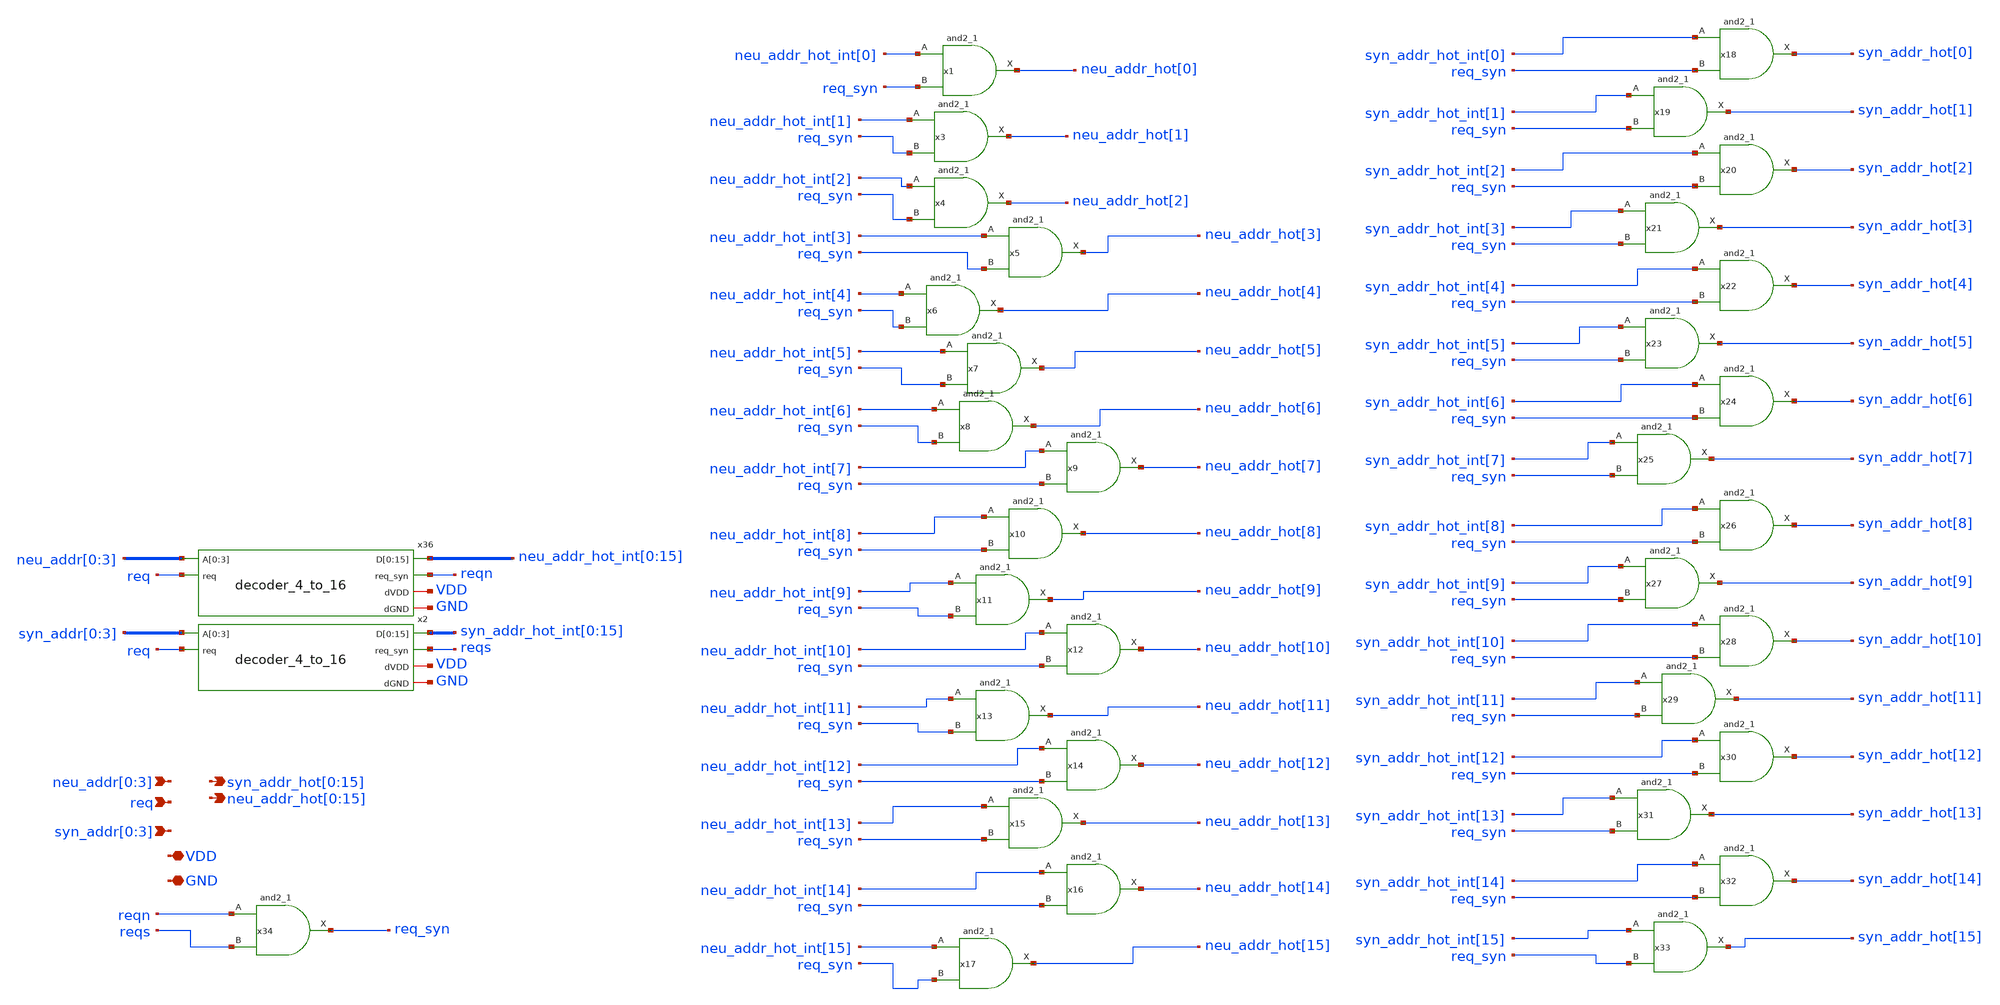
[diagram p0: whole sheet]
** sch_path: design/xschem/neu_syn_addr_decoder.sch
**.subckt neu_syn_addr_decoder neu_addr[0],neu_addr[1],neu_addr[2],neu_addr[3] req
*+ syn_addr_hot[0],syn_addr_hot[1],syn_addr_hot[2],syn_addr_hot[3],syn_addr_hot[4],syn_addr_hot[5],syn_addr_hot[6],syn_addr_hot[7],syn_addr_hot[8],syn_addr_hot[9],syn_addr_hot[10],syn_addr_hot[11],syn_addr_hot[12],syn_addr_hot[13],syn_addr_hot[14],syn_addr_hot[15] syn_addr[0],syn_addr[1],syn_addr[2],syn_addr[3]
*+ neu_addr_hot[0],neu_addr_hot[1],neu_addr_hot[2],neu_addr_hot[3],neu_addr_hot[4],neu_addr_hot[5],neu_addr_hot[6],neu_addr_hot[7],neu_addr_hot[8],neu_addr_hot[9],neu_addr_hot[10],neu_addr_hot[11],neu_addr_hot[12],neu_addr_hot[13],neu_addr_hot[14],neu_addr_hot[15] VDD GND
*.ipin neu_addr[0],neu_addr[1],neu_addr[2],neu_addr[3]
*.ipin req
*.opin
*+ syn_addr_hot[0],syn_addr_hot[1],syn_addr_hot[2],syn_addr_hot[3],syn_addr_hot[4],syn_addr_hot[5],syn_addr_hot[6],syn_addr_hot[7],syn_addr_hot[8],syn_addr_hot[9],syn_addr_hot[10],syn_addr_hot[11],syn_addr_hot[12],syn_addr_hot[13],syn_addr_hot[14],syn_addr_hot[15]
*.ipin syn_addr[0],syn_addr[1],syn_addr[2],syn_addr[3]
*.opin
*+ neu_addr_hot[0],neu_addr_hot[1],neu_addr_hot[2],neu_addr_hot[3],neu_addr_hot[4],neu_addr_hot[5],neu_addr_hot[6],neu_addr_hot[7],neu_addr_hot[8],neu_addr_hot[9],neu_addr_hot[10],neu_addr_hot[11],neu_addr_hot[12],neu_addr_hot[13],neu_addr_hot[14],neu_addr_hot[15]
*.iopin VDD
*.iopin GND
x36 neu_addr[0] neu_addr[1] neu_addr[2] neu_addr[3] neu_addr_hot_int[0] neu_addr_hot_int[1]
+ neu_addr_hot_int[2] neu_addr_hot_int[3] neu_addr_hot_int[4] neu_addr_hot_int[5] neu_addr_hot_int[6] neu_addr_hot_int[7]
+ neu_addr_hot_int[8] neu_addr_hot_int[9] neu_addr_hot_int[10] neu_addr_hot_int[11] neu_addr_hot_int[12]
+ neu_addr_hot_int[13] neu_addr_hot_int[14] neu_addr_hot_int[15] req reqn VDD GND decoder_4_to_16
x2 syn_addr[0] syn_addr[1] syn_addr[2] syn_addr[3] syn_addr_hot_int[0] syn_addr_hot_int[1]
+ syn_addr_hot_int[2] syn_addr_hot_int[3] syn_addr_hot_int[4] syn_addr_hot_int[5] syn_addr_hot_int[6] syn_addr_hot_int[7]
+ syn_addr_hot_int[8] syn_addr_hot_int[9] syn_addr_hot_int[10] syn_addr_hot_int[11] syn_addr_hot_int[12]
+ syn_addr_hot_int[13] syn_addr_hot_int[14] syn_addr_hot_int[15] req reqs VDD GND decoder_4_to_16
x1 neu_addr_hot_int[0] req_syn GND GND VDD VDD neu_addr_hot[0] sky130_fd_sc_hd__and2_1
x3 neu_addr_hot_int[1] req_syn GND GND VDD VDD neu_addr_hot[1] sky130_fd_sc_hd__and2_1
x4 neu_addr_hot_int[2] req_syn GND GND VDD VDD neu_addr_hot[2] sky130_fd_sc_hd__and2_1
x5 neu_addr_hot_int[3] req_syn GND GND VDD VDD neu_addr_hot[3] sky130_fd_sc_hd__and2_1
x6 neu_addr_hot_int[4] req_syn GND GND VDD VDD neu_addr_hot[4] sky130_fd_sc_hd__and2_1
x7 neu_addr_hot_int[5] req_syn GND GND VDD VDD neu_addr_hot[5] sky130_fd_sc_hd__and2_1
x8 neu_addr_hot_int[6] req_syn GND GND VDD VDD neu_addr_hot[6] sky130_fd_sc_hd__and2_1
x9 neu_addr_hot_int[7] req_syn GND GND VDD VDD neu_addr_hot[7] sky130_fd_sc_hd__and2_1
x10 neu_addr_hot_int[8] req_syn GND GND VDD VDD neu_addr_hot[8] sky130_fd_sc_hd__and2_1
x11 neu_addr_hot_int[9] req_syn GND GND VDD VDD neu_addr_hot[9] sky130_fd_sc_hd__and2_1
x12 neu_addr_hot_int[10] req_syn GND GND VDD VDD neu_addr_hot[10] sky130_fd_sc_hd__and2_1
x13 neu_addr_hot_int[11] req_syn GND GND VDD VDD neu_addr_hot[11] sky130_fd_sc_hd__and2_1
x14 neu_addr_hot_int[12] req_syn GND GND VDD VDD neu_addr_hot[12] sky130_fd_sc_hd__and2_1
x15 neu_addr_hot_int[13] req_syn GND GND VDD VDD neu_addr_hot[13] sky130_fd_sc_hd__and2_1
x16 neu_addr_hot_int[14] req_syn GND GND VDD VDD neu_addr_hot[14] sky130_fd_sc_hd__and2_1
x17 neu_addr_hot_int[15] req_syn GND GND VDD VDD neu_addr_hot[15] sky130_fd_sc_hd__and2_1
x18 syn_addr_hot_int[0] req_syn GND GND VDD VDD syn_addr_hot[0] sky130_fd_sc_hd__and2_1
x19 syn_addr_hot_int[1] req_syn GND GND VDD VDD syn_addr_hot[1] sky130_fd_sc_hd__and2_1
x20 syn_addr_hot_int[2] req_syn GND GND VDD VDD syn_addr_hot[2] sky130_fd_sc_hd__and2_1
x21 syn_addr_hot_int[3] req_syn GND GND VDD VDD syn_addr_hot[3] sky130_fd_sc_hd__and2_1
x22 syn_addr_hot_int[4] req_syn GND GND VDD VDD syn_addr_hot[4] sky130_fd_sc_hd__and2_1
x23 syn_addr_hot_int[5] req_syn GND GND VDD VDD syn_addr_hot[5] sky130_fd_sc_hd__and2_1
x24 syn_addr_hot_int[6] req_syn GND GND VDD VDD syn_addr_hot[6] sky130_fd_sc_hd__and2_1
x25 syn_addr_hot_int[7] req_syn GND GND VDD VDD syn_addr_hot[7] sky130_fd_sc_hd__and2_1
x26 syn_addr_hot_int[8] req_syn GND GND VDD VDD syn_addr_hot[8] sky130_fd_sc_hd__and2_1
x27 syn_addr_hot_int[9] req_syn GND GND VDD VDD syn_addr_hot[9] sky130_fd_sc_hd__and2_1
x28 syn_addr_hot_int[10] req_syn GND GND VDD VDD syn_addr_hot[10] sky130_fd_sc_hd__and2_1
x29 syn_addr_hot_int[11] req_syn GND GND VDD VDD syn_addr_hot[11] sky130_fd_sc_hd__and2_1
x30 syn_addr_hot_int[12] req_syn GND GND VDD VDD syn_addr_hot[12] sky130_fd_sc_hd__and2_1
x31 syn_addr_hot_int[13] req_syn GND GND VDD VDD syn_addr_hot[13] sky130_fd_sc_hd__and2_1
x32 syn_addr_hot_int[14] req_syn GND GND VDD VDD syn_addr_hot[14] sky130_fd_sc_hd__and2_1
x33 syn_addr_hot_int[15] req_syn GND GND VDD VDD syn_addr_hot[15] sky130_fd_sc_hd__and2_1
x34 reqn reqs GND GND VDD VDD req_syn sky130_fd_sc_hd__and2_1
**.ends

* expanding   symbol:  decoder_4_to_16.sym # of pins=6
** sym_path: design/xschem/decoder_4_to_16.sym
** sch_path: design/xschem/decoder_4_to_16.sch
.subckt decoder_4_to_16 A[0] A[1] A[2] A[3] D[0] D[1] D[2] D[3] D[4] D[5] D[6] D[7] D[8] D[9] D[10]
+ D[11] D[12] D[13] D[14] D[15] req req_syn dVDD dGND
*.ipin A[0],A[1],A[2],A[3]
*.ipin req
*.opin D[0],D[1],D[2],D[3],D[4],D[5],D[6],D[7],D[8],D[9],D[10],D[11],D[12],D[13],D[14],D[15]
*.opin req_syn
*.iopin dVDD
*.iopin dGND
x21 req dGND dGND dVDD dVDD net5 sky130_fd_sc_hd__inv_1
x22 net5 dGND dGND dVDD dVDD net6 sky130_fd_sc_hd__inv_1
x23 net6 dGND dGND dVDD dVDD net7 sky130_fd_sc_hd__inv_1
x24 net7 dGND dGND dVDD dVDD req_syn sky130_fd_sc_hd__inv_1
x20 A[3] A[2] A[1] A[0] dGND dGND dVDD dVDD D[15] sky130_fd_sc_hd__and4_1
x19 A[3] A[2] A[1] net4 dGND dGND dVDD dVDD D[14] sky130_fd_sc_hd__and4_1
x18 A[3] A[2] net3 A[0] dGND dGND dVDD dVDD D[13] sky130_fd_sc_hd__and4_1
x17 A[3] A[2] net3 net4 dGND dGND dVDD dVDD D[12] sky130_fd_sc_hd__and4_1
x16 A[3] net2 A[1] A[0] dGND dGND dVDD dVDD D[11] sky130_fd_sc_hd__and4_1
x15 A[3] net2 A[1] net4 dGND dGND dVDD dVDD D[10] sky130_fd_sc_hd__and4_1
x13 A[3] net2 net3 A[0] dGND dGND dVDD dVDD D[9] sky130_fd_sc_hd__and4_1
x4 A[3] net2 net3 net4 dGND dGND dVDD dVDD D[8] sky130_fd_sc_hd__and4_1
x5 net1 A[2] A[1] A[0] dGND dGND dVDD dVDD D[7] sky130_fd_sc_hd__and4_1
x6 net1 A[2] A[1] net4 dGND dGND dVDD dVDD D[6] sky130_fd_sc_hd__and4_1
x8 net1 A[2] net3 net4 dGND dGND dVDD dVDD D[4] sky130_fd_sc_hd__and4_1
x9 net1 net2 A[1] net4 dGND dGND dVDD dVDD D[2] sky130_fd_sc_hd__and4_1
x10 net1 net2 net3 net4 dGND dGND dVDD dVDD D[0] sky130_fd_sc_hd__and4_1
x11 net1 net2 net3 A[0] dGND dGND dVDD dVDD D[1] sky130_fd_sc_hd__and4_1
x12 net1 net2 A[1] A[0] dGND dGND dVDD dVDD D[3] sky130_fd_sc_hd__and4_1
x14 net1 A[2] net3 A[0] dGND dGND dVDD dVDD D[5] sky130_fd_sc_hd__and4_1
x1 A[3] dGND dGND dVDD dVDD net1 sky130_fd_sc_hd__inv_4
x2 A[2] dGND dGND dVDD dVDD net2 sky130_fd_sc_hd__inv_4
x3 A[1] dGND dGND dVDD dVDD net3 sky130_fd_sc_hd__inv_4
x7 A[0] dGND dGND dVDD dVDD net4 sky130_fd_sc_hd__inv_4
.ends

.end
